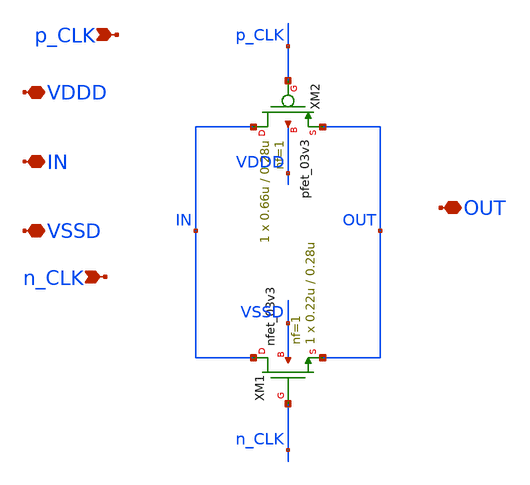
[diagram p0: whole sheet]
** sch_path: SAR_ADC/blocks/SAR_logic/t_gate.sch
**.subckt t_gate IN VDDD VSSD OUT n_CLK p_CLK
*.iopin IN
*.iopin VDDD
*.iopin VSSD
*.iopin OUT
*.ipin n_CLK
*.ipin p_CLK
XM1 IN n_CLK OUT VSSD nfet_03v3 L=0.28u W=0.22u nf=1 ad='int((nf+1)/2) * W/nf * 0.18u' as='int((nf+2)/2) * W/nf * 0.18u'
+ pd='2*int((nf+1)/2) * (W/nf + 0.18u)' ps='2*int((nf+2)/2) * (W/nf + 0.18u)' nrd='0.18u / W' nrs='0.18u / W'
+ sa=0 sb=0 sd=0 m=1
XM2 IN p_CLK OUT VDDD pfet_03v3 L=0.28u W=0.66u nf=1 ad='int((nf+1)/2) * W/nf * 0.18u' as='int((nf+2)/2) * W/nf * 0.18u'
+ pd='2*int((nf+1)/2) * (W/nf + 0.18u)' ps='2*int((nf+2)/2) * (W/nf + 0.18u)' nrd='0.18u / W' nrs='0.18u / W'
+ sa=0 sb=0 sd=0 m=1
**.ends
.end
